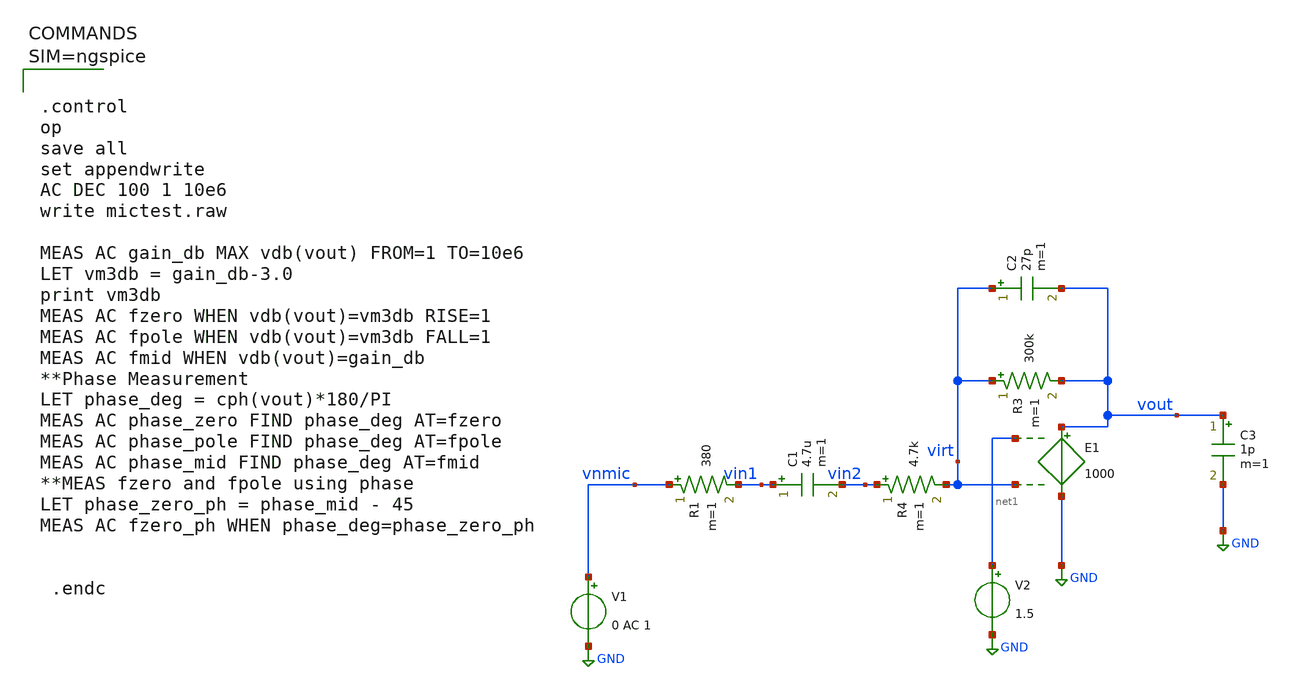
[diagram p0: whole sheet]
** sch_path: xschem/mictest.sch
**.subckt mictest
V1 vnmic GND 0 AC 1
R1 vnmic vin1 380 m=1
C1 vin1 vin2 4.7u m=1
E1 vout GND net1 virt 1000
R3 virt vout 300k m=1
C2 virt vout 27p m=1
V2 net1 GND 1.5
C3 vout GND 1p m=1
R4 vin2 virt 4.7k m=1
**** begin user architecture code



.control
op
save all
set appendwrite
AC DEC 100 1 10e6
write mictest.raw

MEAS AC gain_db MAX vdb(vout) FROM=1 TO=10e6
LET vm3db = gain_db-3.0
print vm3db
MEAS AC fzero WHEN vdb(vout)=vm3db RISE=1
MEAS AC fpole WHEN vdb(vout)=vm3db FALL=1
MEAS AC fmid WHEN vdb(vout)=gain_db
**Phase Measurement
LET phase_deg = cph(vout)*180/PI
MEAS AC phase_zero FIND phase_deg AT=fzero
MEAS AC phase_pole FIND phase_deg AT=fpole
MEAS AC phase_mid FIND phase_deg AT=fmid
**MEAS fzero and fpole using phase
LET phase_zero_ph = phase_mid - 45
MEAS AC fzero_ph WHEN phase_deg=phase_zero_ph


 .endc



**** end user architecture code
**.ends
.GLOBAL GND
.end
